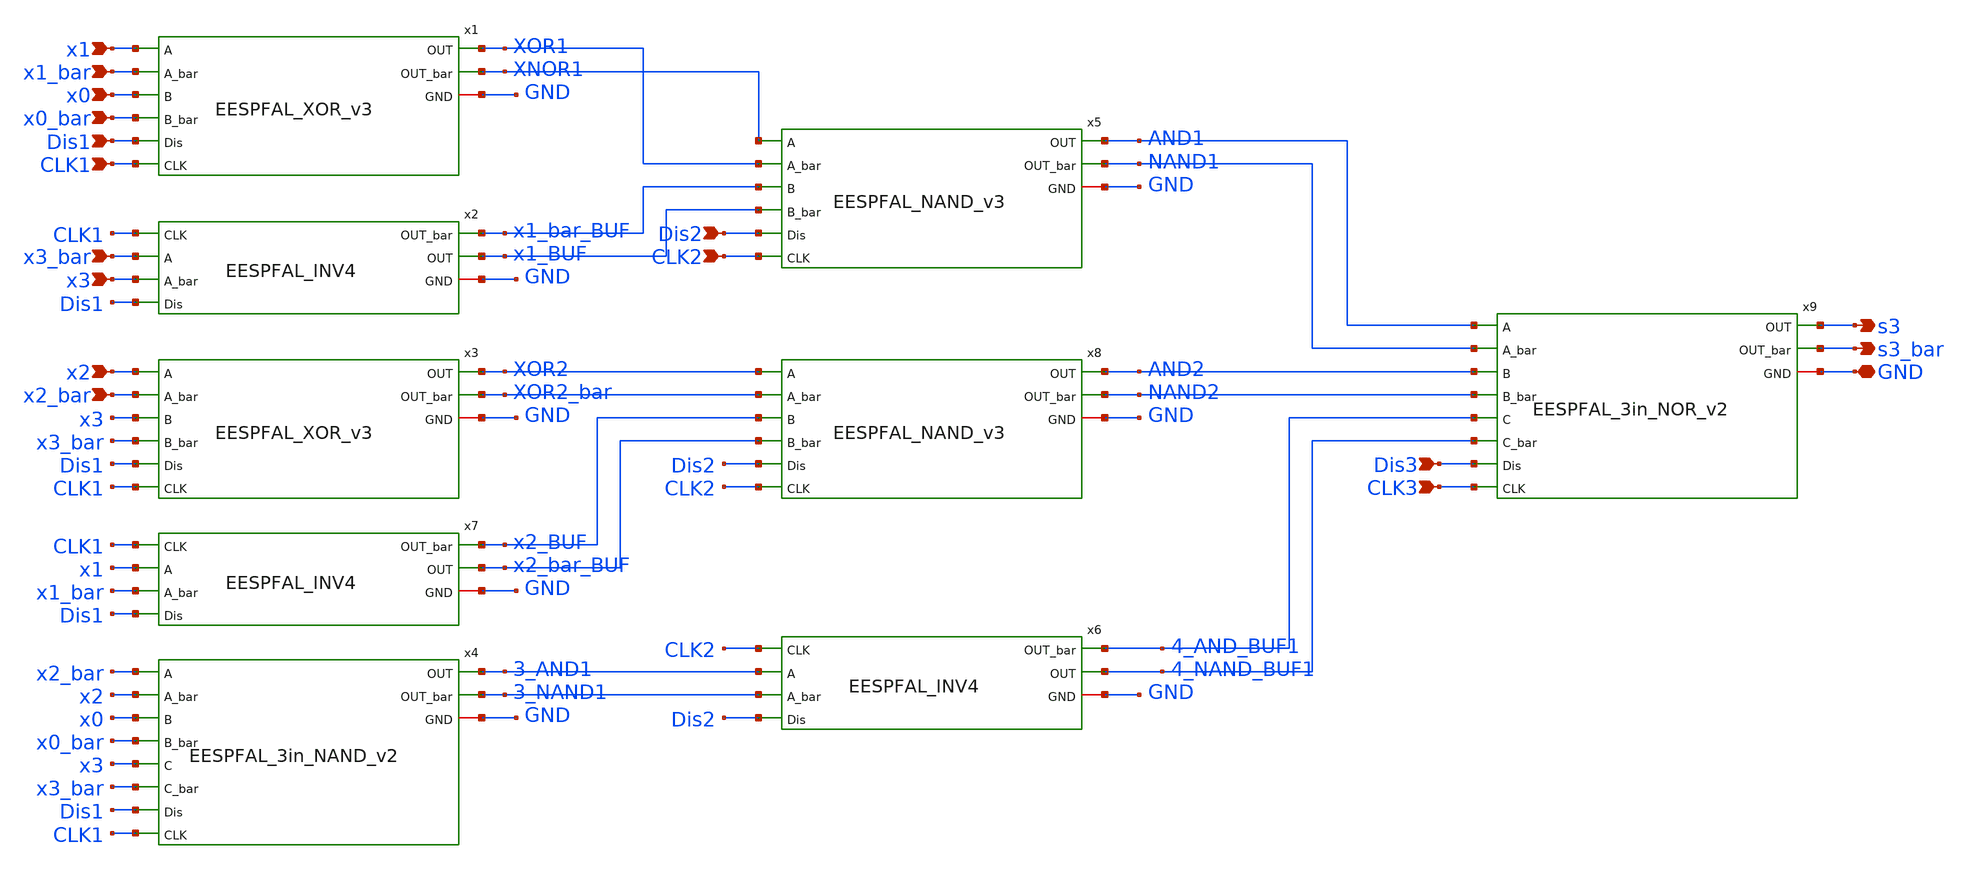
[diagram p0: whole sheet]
** sch_path: skywater_stuff/EESPFAL_s3_magic_checked.sch
**.subckt EESPFAL_s3_magic_checked x0 x0_bar x1 x1_bar x2 x2_bar x3 x3_bar s3 s3_bar Dis1 Dis2 Dis3
*+ GND CLK1 CLK2 CLK3
*.ipin x0
*.ipin x0_bar
*.ipin x1
*.ipin x1_bar
*.ipin x2
*.ipin x2_bar
*.ipin x3
*.ipin x3_bar
*.opin s3
*.opin s3_bar
*.ipin Dis1
*.ipin Dis2
*.ipin Dis3
*.iopin GND
*.ipin CLK1
*.ipin CLK2
*.ipin CLK3
x9 AND1 NAND1 AND2 NAND2 4_AND_BUF1 4_NAND_BUF1 s3 s3_bar Dis3 GND CLK3 EESPFAL_3in_NOR_v2
x4 x2_bar x2 x0 x0_bar x3 x3_bar 3_AND1 3_NAND1 Dis1 GND CLK1 EESPFAL_3in_NAND_v2
x1 x1 x1_bar x0 x0_bar XOR1 XNOR1 Dis1 GND CLK1 EESPFAL_XOR_v3
x2 x3_bar x3 x1_BUF x1_bar_BUF Dis1 GND CLK1 EESPFAL_INV4
x3 x2 x2_bar x3 x3_bar XOR2 XOR2_bar Dis1 GND CLK1 EESPFAL_XOR_v3
x7 x1 x1_bar x2_bar_BUF x2_BUF Dis1 GND CLK1 EESPFAL_INV4
x6 3_AND1 3_NAND1 4_NAND_BUF1 4_AND_BUF1 Dis2 GND CLK2 EESPFAL_INV4
x8 XOR2 XOR2_bar x2_BUF x2_bar_BUF AND2 NAND2 Dis2 GND CLK2 EESPFAL_NAND_v3
x5 XNOR1 XOR1 x1_bar_BUF x1_BUF AND1 NAND1 Dis2 GND CLK2 EESPFAL_NAND_v3
**.ends
.end
